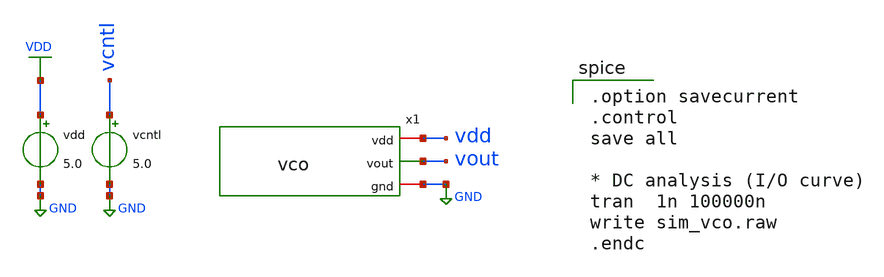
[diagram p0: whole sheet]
** sch_path: xschem/sim_vco.sch
**.subckt sim_vco
vcntl vcntl GND 5.0
vdd VDD GND 5.0
x1 vdd vout GND vco
**** begin user architecture code
 .include $::LIB/mos.lib
.include $::LIB/passive.lib
.include $::LIB/diode.lib

.option savecurrent
.control
save all

* DC analysis (I/O curve)
tran  1n 100000n
write sim_vco.raw
.endc

**** end user architecture code
**.ends
.GLOBAL GND
.GLOBAL VDD
.end
